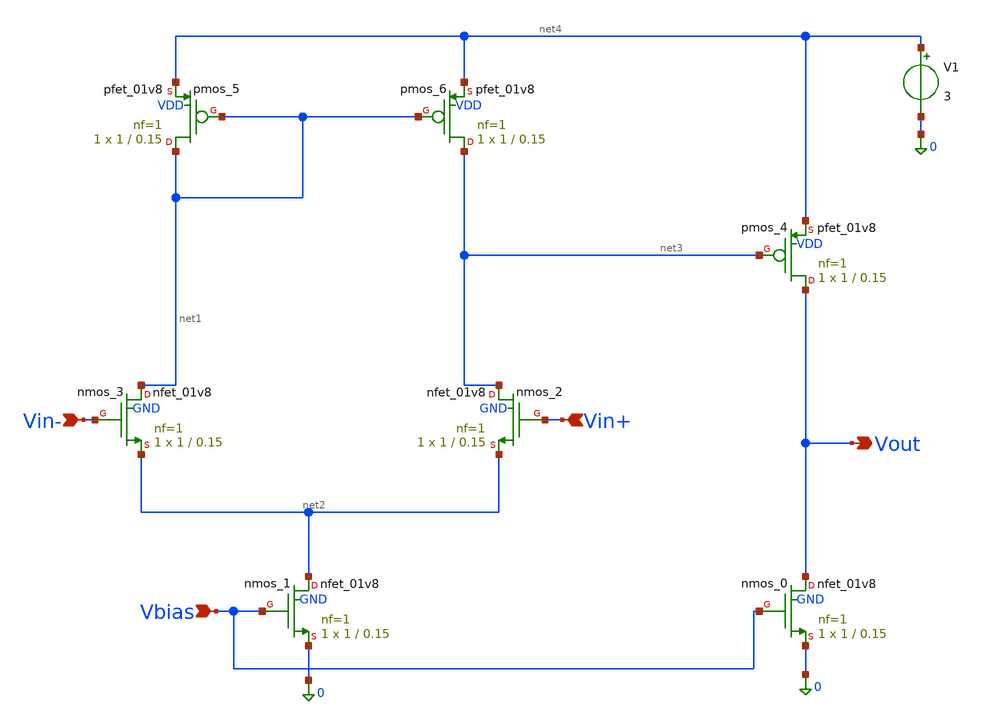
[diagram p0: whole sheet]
** sch_path: golden_netlists/10_1007_s00034-017-0630-6_03_001_crop1.sch
**.subckt 10_1007_s00034-017-0630-6_03_001_crop1 Vbias Vin- Vin+ Vout
*.ipin Vbias
*.ipin Vin-
*.ipin Vin+
*.opin Vout
Xnmos_0 Vout Vbias 0 GND sky130_fd_pr__nfet_01v8 L=0.15 W=1 nf=1 ad='int((nf+1)/2) * W/nf * 0.29' as='int((nf+2)/2) * W/nf * 0.29'
+ pd='2*int((nf+1)/2) * (W/nf + 0.29)' ps='2*int((nf+2)/2) * (W/nf + 0.29)' nrd='0.29 / W' nrs='0.29 / W'
+ sa=0 sb=0 sd=0 mult=1 m=1
Xnmos_1 net2 Vbias 0 GND sky130_fd_pr__nfet_01v8 L=0.15 W=1 nf=1 ad='int((nf+1)/2) * W/nf * 0.29' as='int((nf+2)/2) * W/nf * 0.29'
+ pd='2*int((nf+1)/2) * (W/nf + 0.29)' ps='2*int((nf+2)/2) * (W/nf + 0.29)' nrd='0.29 / W' nrs='0.29 / W'
+ sa=0 sb=0 sd=0 mult=1 m=1
Xnmos_2 net3 Vin+ net2 GND sky130_fd_pr__nfet_01v8 L=0.15 W=1 nf=1 ad='int((nf+1)/2) * W/nf * 0.29' as='int((nf+2)/2) * W/nf * 0.29'
+ pd='2*int((nf+1)/2) * (W/nf + 0.29)' ps='2*int((nf+2)/2) * (W/nf + 0.29)' nrd='0.29 / W' nrs='0.29 / W'
+ sa=0 sb=0 sd=0 mult=1 m=1
Xnmos_3 net1 Vin- net2 GND sky130_fd_pr__nfet_01v8 L=0.15 W=1 nf=1 ad='int((nf+1)/2) * W/nf * 0.29' as='int((nf+2)/2) * W/nf * 0.29'
+ pd='2*int((nf+1)/2) * (W/nf + 0.29)' ps='2*int((nf+2)/2) * (W/nf + 0.29)' nrd='0.29 / W' nrs='0.29 / W'
+ sa=0 sb=0 sd=0 mult=1 m=1
Xpmos_4 Vout net3 net4 VDD sky130_fd_pr__pfet_01v8 L=0.15 W=1 nf=1 ad='int((1 + 1)/2) * 1 / 1 * 0.29'
+ as='int((1 + 2)/2) * 1 / 1 * 0.29' pd='2*int((1 + 1)/2) * (1 / 1 + 0.29)' ps='2*int((1 + 2)/2) * (1 / 1 + 0.29)'
+ nrd='0.29 / 1 ' nrs='0.29 / 1 ' sa=0 sb=0 sd=0 mult=1 m=1
Xpmos_5 net1 net1 net4 VDD sky130_fd_pr__pfet_01v8 L=0.15 W=1 nf=1 ad='int((1 + 1)/2) * 1 / 1 * 0.29'
+ as='int((1 + 2)/2) * 1 / 1 * 0.29' pd='2*int((1 + 1)/2) * (1 / 1 + 0.29)' ps='2*int((1 + 2)/2) * (1 / 1 + 0.29)'
+ nrd='0.29 / 1 ' nrs='0.29 / 1 ' sa=0 sb=0 sd=0 mult=1 m=1
Xpmos_6 net3 net1 net4 VDD sky130_fd_pr__pfet_01v8 L=0.15 W=1 nf=1 ad='int((1 + 1)/2) * 1 / 1 * 0.29'
+ as='int((1 + 2)/2) * 1 / 1 * 0.29' pd='2*int((1 + 1)/2) * (1 / 1 + 0.29)' ps='2*int((1 + 2)/2) * (1 / 1 + 0.29)'
+ nrd='0.29 / 1 ' nrs='0.29 / 1 ' sa=0 sb=0 sd=0 mult=1 m=1
V1 net4 0 3
**.ends
.end
